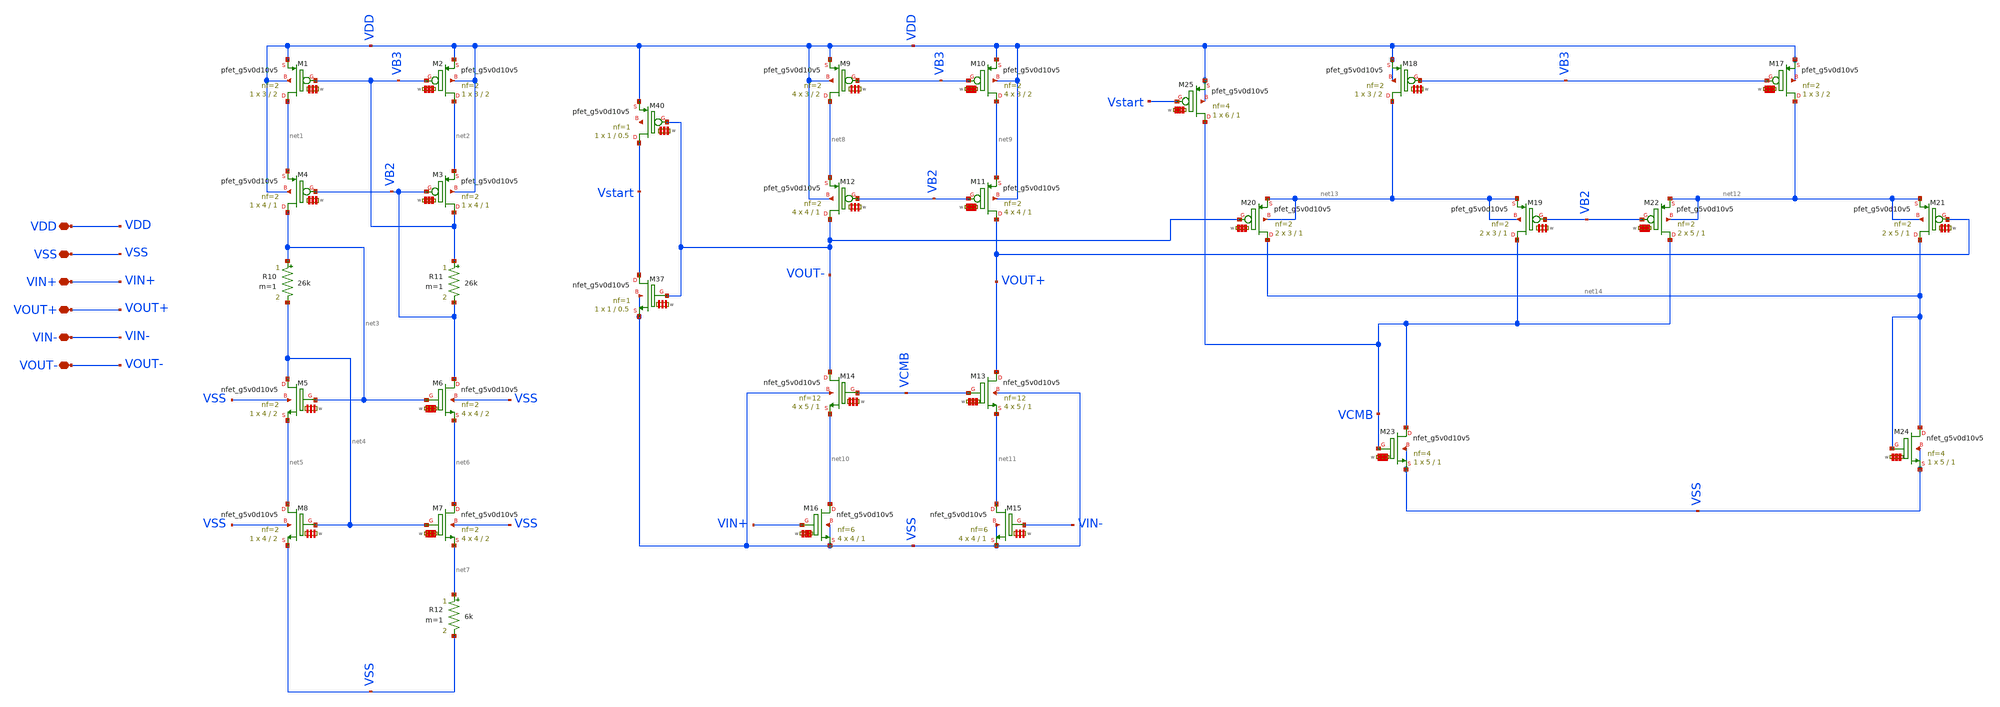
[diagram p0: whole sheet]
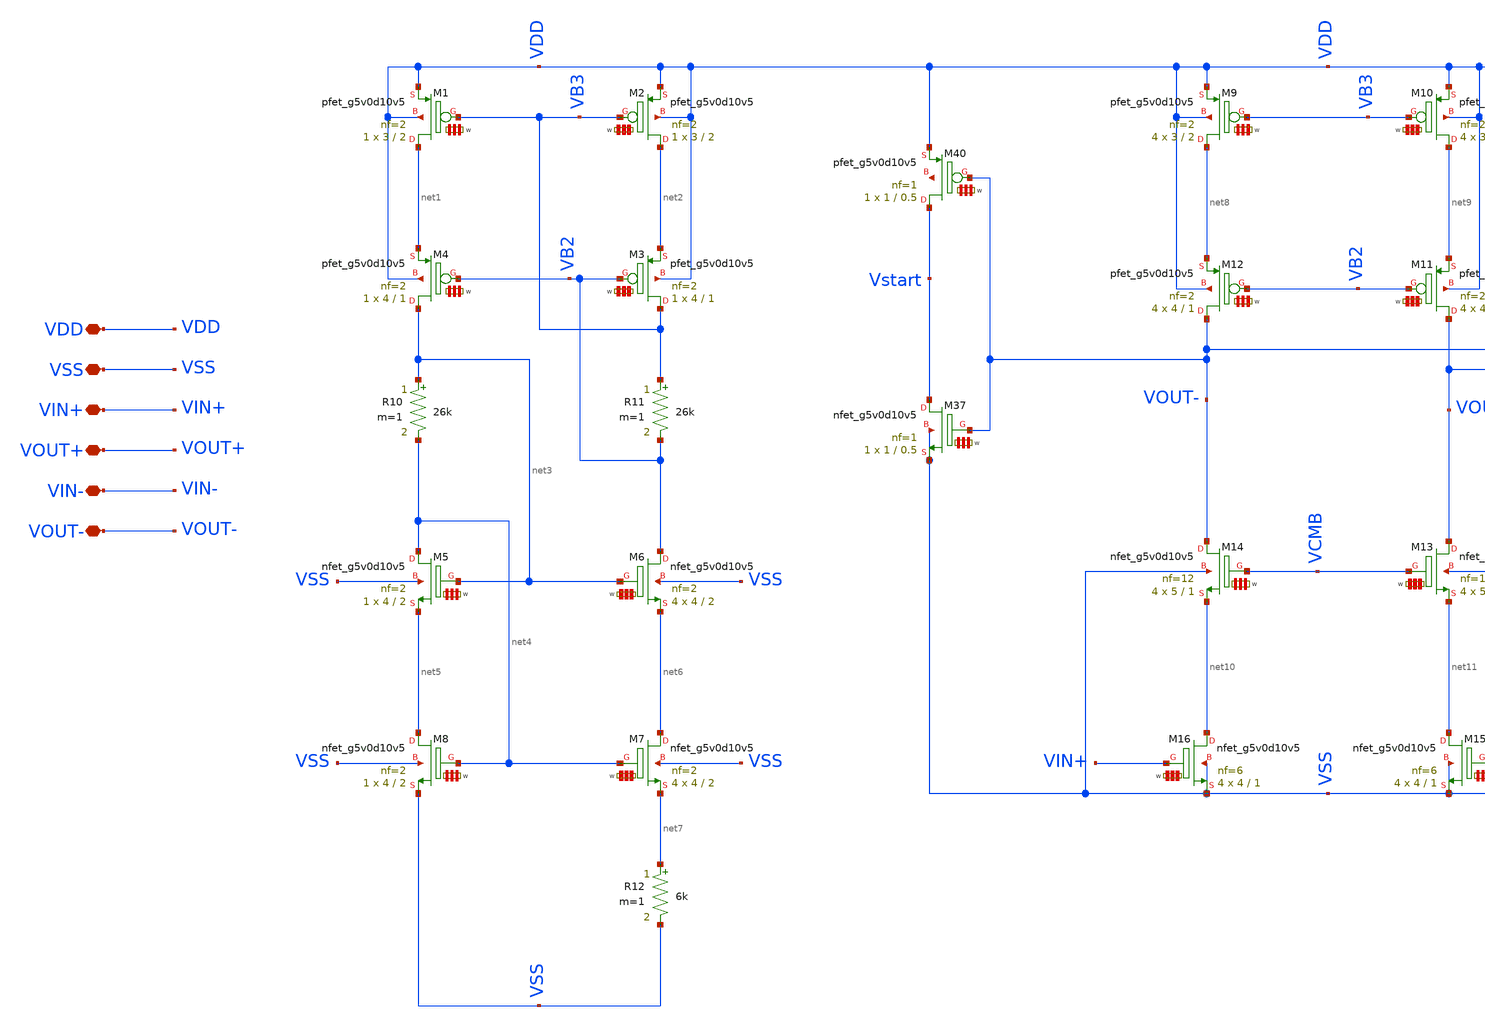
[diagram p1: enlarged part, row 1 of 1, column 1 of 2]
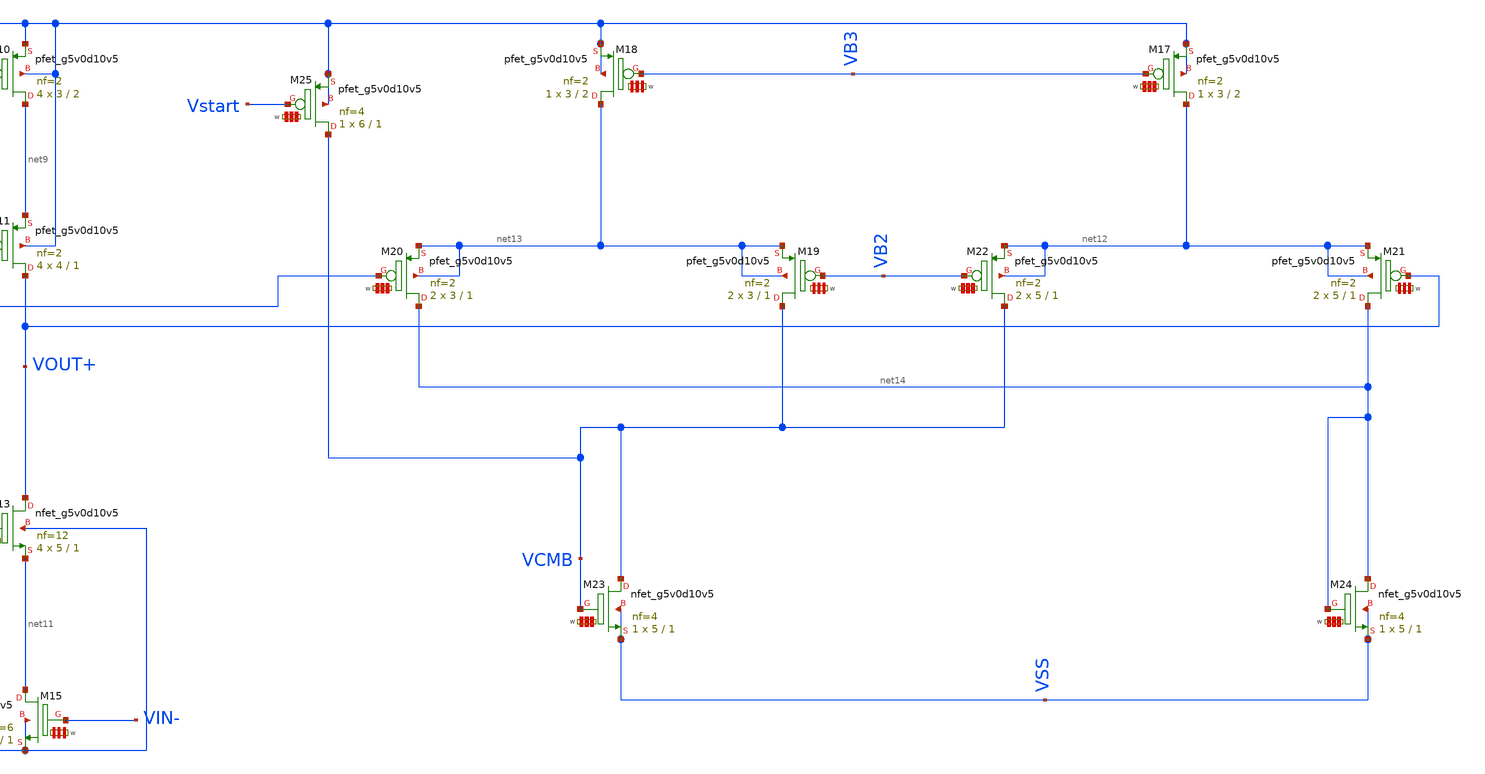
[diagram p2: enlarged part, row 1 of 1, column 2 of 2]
** sch_path: my_ip/sky130A/fully_differential_telescopic_cascode_5V_V1/fd_opamp.sch
**.subckt fd_opamp VDD VSS VIN+ VOUT+ VIN- VOUT-
*.iopin VDD
*.iopin VSS
*.iopin VIN+
*.iopin VOUT+
*.iopin VIN-
*.iopin VOUT-
XM1 net1 VB3 VDD VDD sky130_fd_pr__pfet_g5v0d10v5 L=2 W='3 * 2 ' nf=2 ad='int((2 + 1)/2) * 3 * 0.29'
+ as='int((2 + 2)/2) * 3 * 0.29' pd='2*int((2 + 1)/2) * (3 + 0.29)' ps='2*int((2 + 2)/2) * (3 + 0.29)'
+ nrd='0.29 / 3 / 2 ' nrs='0.29 / 3 / 2 ' sa=0 sb=0 sd=0 mult=1 m=1
XM3 VB3 VB2 net2 VDD sky130_fd_pr__pfet_g5v0d10v5 L=1 W='4 * 2 ' nf=2 ad='int((2 + 1)/2) * 4 * 0.29'
+ as='int((2 + 2)/2) * 4 * 0.29' pd='2*int((2 + 1)/2) * (4 + 0.29)' ps='2*int((2 + 2)/2) * (4 + 0.29)'
+ nrd='0.29 / 4 / 2 ' nrs='0.29 / 4 / 2 ' sa=0 sb=0 sd=0 mult=1 m=1
R10 net3 net4 26k m=1
R11 VB3 VB2 26k m=1
XM7 net6 net4 net7 VSS sky130_fd_pr__nfet_g5v0d10v5 L=2 W='4 * 2 ' nf=2 ad='int((nf+1)/2) * W / nf * 0.29'
+ as='int((nf+2)/2) * W / nf * 0.29' pd='2*int((nf+1)/2) * (W / nf + 0.29)' ps='2*int((nf+2)/2) * (W / nf + 0.29)'
+ nrd='0.29 / W ' nrs='0.29 / W ' sa=0 sb=0 sd=0 mult=4 m=4
R12 net7 VSS 6k m=1
XM2 net2 VB3 VDD VDD sky130_fd_pr__pfet_g5v0d10v5 L=2 W='3 * 2 ' nf=2 ad='int((2 + 1)/2) * 3 * 0.29'
+ as='int((2 + 2)/2) * 3 * 0.29' pd='2*int((2 + 1)/2) * (3 + 0.29)' ps='2*int((2 + 2)/2) * (3 + 0.29)'
+ nrd='0.29 / 3 / 2 ' nrs='0.29 / 3 / 2 ' sa=0 sb=0 sd=0 mult=1 m=1
XM6 VB2 net3 net6 VSS sky130_fd_pr__nfet_g5v0d10v5 L=2 W='4 * 2 ' nf=2 ad='int((nf+1)/2) * W / nf * 0.29'
+ as='int((nf+2)/2) * W / nf * 0.29' pd='2*int((nf+1)/2) * (W / nf + 0.29)' ps='2*int((nf+2)/2) * (W / nf + 0.29)'
+ nrd='0.29 / W ' nrs='0.29 / W ' sa=0 sb=0 sd=0 mult=4 m=4
XM5 net4 net3 net5 VSS sky130_fd_pr__nfet_g5v0d10v5 L=2 W='4 * 2 ' nf=2 ad='int((nf+1)/2) * W / nf * 0.29'
+ as='int((nf+2)/2) * W / nf * 0.29' pd='2*int((nf+1)/2) * (W / nf + 0.29)' ps='2*int((nf+2)/2) * (W / nf + 0.29)'
+ nrd='0.29 / W ' nrs='0.29 / W ' sa=0 sb=0 sd=0 mult=1 m=1
XM8 net5 net4 VSS VSS sky130_fd_pr__nfet_g5v0d10v5 L=2 W='4 * 2 ' nf=2 ad='int((nf+1)/2) * W / nf * 0.29'
+ as='int((nf+2)/2) * W / nf * 0.29' pd='2*int((nf+1)/2) * (W / nf + 0.29)' ps='2*int((nf+2)/2) * (W / nf + 0.29)'
+ nrd='0.29 / W ' nrs='0.29 / W ' sa=0 sb=0 sd=0 mult=1 m=1
XM4 net3 VB2 net1 VDD sky130_fd_pr__pfet_g5v0d10v5 L=1 W='4 * 2 ' nf=2 ad='int((2 + 1)/2) * 4 * 0.29'
+ as='int((2 + 2)/2) * 4 * 0.29' pd='2*int((2 + 1)/2) * (4 + 0.29)' ps='2*int((2 + 2)/2) * (4 + 0.29)'
+ nrd='0.29 / 4 / 2 ' nrs='0.29 / 4 / 2 ' sa=0 sb=0 sd=0 mult=1 m=1
XM9 net8 VB3 VDD VDD sky130_fd_pr__pfet_g5v0d10v5 L=2 W='3 * 2 ' nf=2 ad='int((2 + 1)/2) * 3 * 0.29'
+ as='int((2 + 2)/2) * 3 * 0.29' pd='2*int((2 + 1)/2) * (3 + 0.29)' ps='2*int((2 + 2)/2) * (3 + 0.29)'
+ nrd='0.29 / 3 / 2 ' nrs='0.29 / 3 / 2 ' sa=0 sb=0 sd=0 mult=4 m=4
XM10 net9 VB3 VDD VDD sky130_fd_pr__pfet_g5v0d10v5 L=2 W='3 * 2 ' nf=2 ad='int((2 + 1)/2) * 3 * 0.29'
+ as='int((2 + 2)/2) * 3 * 0.29' pd='2*int((2 + 1)/2) * (3 + 0.29)' ps='2*int((2 + 2)/2) * (3 + 0.29)'
+ nrd='0.29 / 3 / 2 ' nrs='0.29 / 3 / 2 ' sa=0 sb=0 sd=0 mult=4 m=4
XM11 VOUT+ VB2 net9 VDD sky130_fd_pr__pfet_g5v0d10v5 L=1 W='4 * 2 ' nf=2 ad='int((2 + 1)/2) * 4 * 0.29'
+ as='int((2 + 2)/2) * 4 * 0.29' pd='2*int((2 + 1)/2) * (4 + 0.29)' ps='2*int((2 + 2)/2) * (4 + 0.29)'
+ nrd='0.29 / 4 / 2 ' nrs='0.29 / 4 / 2 ' sa=0 sb=0 sd=0 mult=4 m=4
XM12 VOUT- VB2 net8 VDD sky130_fd_pr__pfet_g5v0d10v5 L=1 W='4 * 2 ' nf=2 ad='int((2 + 1)/2) * 4 * 0.29'
+ as='int((2 + 2)/2) * 4 * 0.29' pd='2*int((2 + 1)/2) * (4 + 0.29)' ps='2*int((2 + 2)/2) * (4 + 0.29)'
+ nrd='0.29 / 4 / 2 ' nrs='0.29 / 4 / 2 ' sa=0 sb=0 sd=0 mult=4 m=4
XM13 VOUT+ VCMB net11 VSS sky130_fd_pr__nfet_g5v0d10v5 L=1 W='5 * 12 ' nf=12 ad='int((nf+1)/2) * W / nf * 0.29'
+ as='int((nf+2)/2) * W / nf * 0.29' pd='2*int((nf+1)/2) * (W / nf + 0.29)' ps='2*int((nf+2)/2) * (W / nf + 0.29)'
+ nrd='0.29 / W ' nrs='0.29 / W ' sa=0 sb=0 sd=0 mult=4 m=4
XM14 VOUT- VCMB net10 VSS sky130_fd_pr__nfet_g5v0d10v5 L=1 W='5 * 12 ' nf=12 ad='int((nf+1)/2) * W / nf * 0.29'
+ as='int((nf+2)/2) * W / nf * 0.29' pd='2*int((nf+1)/2) * (W / nf + 0.29)' ps='2*int((nf+2)/2) * (W / nf + 0.29)'
+ nrd='0.29 / W ' nrs='0.29 / W ' sa=0 sb=0 sd=0 mult=4 m=4
XM15 net11 VIN- VSS VSS sky130_fd_pr__nfet_g5v0d10v5 L=1 W='4 * 6 ' nf=6 ad='int((nf+1)/2) * W / nf * 0.29'
+ as='int((nf+2)/2) * W / nf * 0.29' pd='2*int((nf+1)/2) * (W / nf + 0.29)' ps='2*int((nf+2)/2) * (W / nf + 0.29)'
+ nrd='0.29 / W ' nrs='0.29 / W ' sa=0 sb=0 sd=0 mult=4 m=4
XM17 net12 VB3 VDD VDD sky130_fd_pr__pfet_g5v0d10v5 L=2 W='3 * 2 ' nf=2 ad='int((2 + 1)/2) * 3 * 0.29'
+ as='int((2 + 2)/2) * 3 * 0.29' pd='2*int((2 + 1)/2) * (3 + 0.29)' ps='2*int((2 + 2)/2) * (3 + 0.29)'
+ nrd='0.29 / 3 / 2 ' nrs='0.29 / 3 / 2 ' sa=0 sb=0 sd=0 mult=1 m=1
XM18 net13 VB3 VDD VDD sky130_fd_pr__pfet_g5v0d10v5 L=2 W='3 * 2 ' nf=2 ad='int((2 + 1)/2) * 3 * 0.29'
+ as='int((2 + 2)/2) * 3 * 0.29' pd='2*int((2 + 1)/2) * (3 + 0.29)' ps='2*int((2 + 2)/2) * (3 + 0.29)'
+ nrd='0.29 / 3 / 2 ' nrs='0.29 / 3 / 2 ' sa=0 sb=0 sd=0 mult=1 m=1
XM19 VCMB VB2 net13 net13 sky130_fd_pr__pfet_g5v0d10v5 L=1 W='3 * 2 ' nf=2 ad='int((2 + 1)/2) * 3 * 0.29'
+ as='int((2 + 2)/2) * 3 * 0.29' pd='2*int((2 + 1)/2) * (3 + 0.29)' ps='2*int((2 + 2)/2) * (3 + 0.29)'
+ nrd='0.29 / 3 / 2 ' nrs='0.29 / 3 / 2 ' sa=0 sb=0 sd=0 mult=2 m=2
XM20 net14 VOUT- net13 net13 sky130_fd_pr__pfet_g5v0d10v5 L=1 W='3 * 2 ' nf=2 ad='int((2 + 1)/2) * 3 * 0.29'
+ as='int((2 + 2)/2) * 3 * 0.29' pd='2*int((2 + 1)/2) * (3 + 0.29)' ps='2*int((2 + 2)/2) * (3 + 0.29)'
+ nrd='0.29 / 3 / 2 ' nrs='0.29 / 3 / 2 ' sa=0 sb=0 sd=0 mult=2 m=2
XM21 net14 VOUT+ net12 net12 sky130_fd_pr__pfet_g5v0d10v5 L=1 W='5 * 2 ' nf=2 ad='int((2 + 1)/2) * 5 * 0.29'
+ as='int((2 + 2)/2) * 5 * 0.29' pd='2*int((2 + 1)/2) * (5 + 0.29)' ps='2*int((2 + 2)/2) * (5 + 0.29)'
+ nrd='0.29 / 5 / 2 ' nrs='0.29 / 5 / 2 ' sa=0 sb=0 sd=0 mult=2 m=2
XM22 VCMB VB2 net12 net12 sky130_fd_pr__pfet_g5v0d10v5 L=1 W='5 * 2 ' nf=2 ad='int((2 + 1)/2) * 5 * 0.29'
+ as='int((2 + 2)/2) * 5 * 0.29' pd='2*int((2 + 1)/2) * (5 + 0.29)' ps='2*int((2 + 2)/2) * (5 + 0.29)'
+ nrd='0.29 / 5 / 2 ' nrs='0.29 / 5 / 2 ' sa=0 sb=0 sd=0 mult=2 m=2
XM16 net10 VIN+ VSS VSS sky130_fd_pr__nfet_g5v0d10v5 L=1 W='4 * 6 ' nf=6 ad='int((nf+1)/2) * W / nf * 0.29'
+ as='int((nf+2)/2) * W / nf * 0.29' pd='2*int((nf+1)/2) * (W / nf + 0.29)' ps='2*int((nf+2)/2) * (W / nf + 0.29)'
+ nrd='0.29 / W ' nrs='0.29 / W ' sa=0 sb=0 sd=0 mult=4 m=4
XM23 VCMB VCMB VSS VSS sky130_fd_pr__nfet_g5v0d10v5 L=1 W='5 * 4 ' nf=4 ad='int((nf+1)/2) * W / nf * 0.29'
+ as='int((nf+2)/2) * W / nf * 0.29' pd='2*int((nf+1)/2) * (W / nf + 0.29)' ps='2*int((nf+2)/2) * (W / nf + 0.29)'
+ nrd='0.29 / W ' nrs='0.29 / W ' sa=0 sb=0 sd=0 mult=1 m=1
XM24 net14 net14 VSS VSS sky130_fd_pr__nfet_g5v0d10v5 L=1 W='5 * 4 ' nf=4 ad='int((nf+1)/2) * W / nf * 0.29'
+ as='int((nf+2)/2) * W / nf * 0.29' pd='2*int((nf+1)/2) * (W / nf + 0.29)' ps='2*int((nf+2)/2) * (W / nf + 0.29)'
+ nrd='0.29 / W ' nrs='0.29 / W ' sa=0 sb=0 sd=0 mult=1 m=1
XM40 Vstart VOUT- VDD net15 sky130_fd_pr__pfet_g5v0d10v5 L=0.5 W='1 * 1 ' nf=1 ad='int((1 + 1)/2) * 1 * 0.29'
+ as='int((1 + 2)/2) * 1 * 0.29' pd='2*int((1 + 1)/2) * (1 + 0.29)' ps='2*int((1 + 2)/2) * (1 + 0.29)'
+ nrd='0.29 / 1 / 1 ' nrs='0.29 / 1 / 1 ' sa=0 sb=0 sd=0 mult=1 m=1
XM37 Vstart VOUT- VSS VSS sky130_fd_pr__nfet_g5v0d10v5 L=0.5 W='1 * 1 ' nf=1 ad='int((nf+1)/2) * W / nf * 0.29'
+ as='int((nf+2)/2) * W / nf * 0.29' pd='2*int((nf+1)/2) * (W / nf + 0.29)' ps='2*int((nf+2)/2) * (W / nf + 0.29)'
+ nrd='0.29 / W ' nrs='0.29 / W ' sa=0 sb=0 sd=0 mult=1 m=1
XM25 VCMB Vstart VDD VDD sky130_fd_pr__pfet_g5v0d10v5 L=1 W='6 * 4 ' nf=4 ad='int((4 + 1)/2) * 6 * 0.29'
+ as='int((4 + 2)/2) * 6 * 0.29' pd='2*int((4 + 1)/2) * (6 + 0.29)' ps='2*int((4 + 2)/2) * (6 + 0.29)'
+ nrd='0.29 / 6 / 4 ' nrs='0.29 / 6 / 4 ' sa=0 sb=0 sd=0 mult=1 m=1
**.ends
.end
